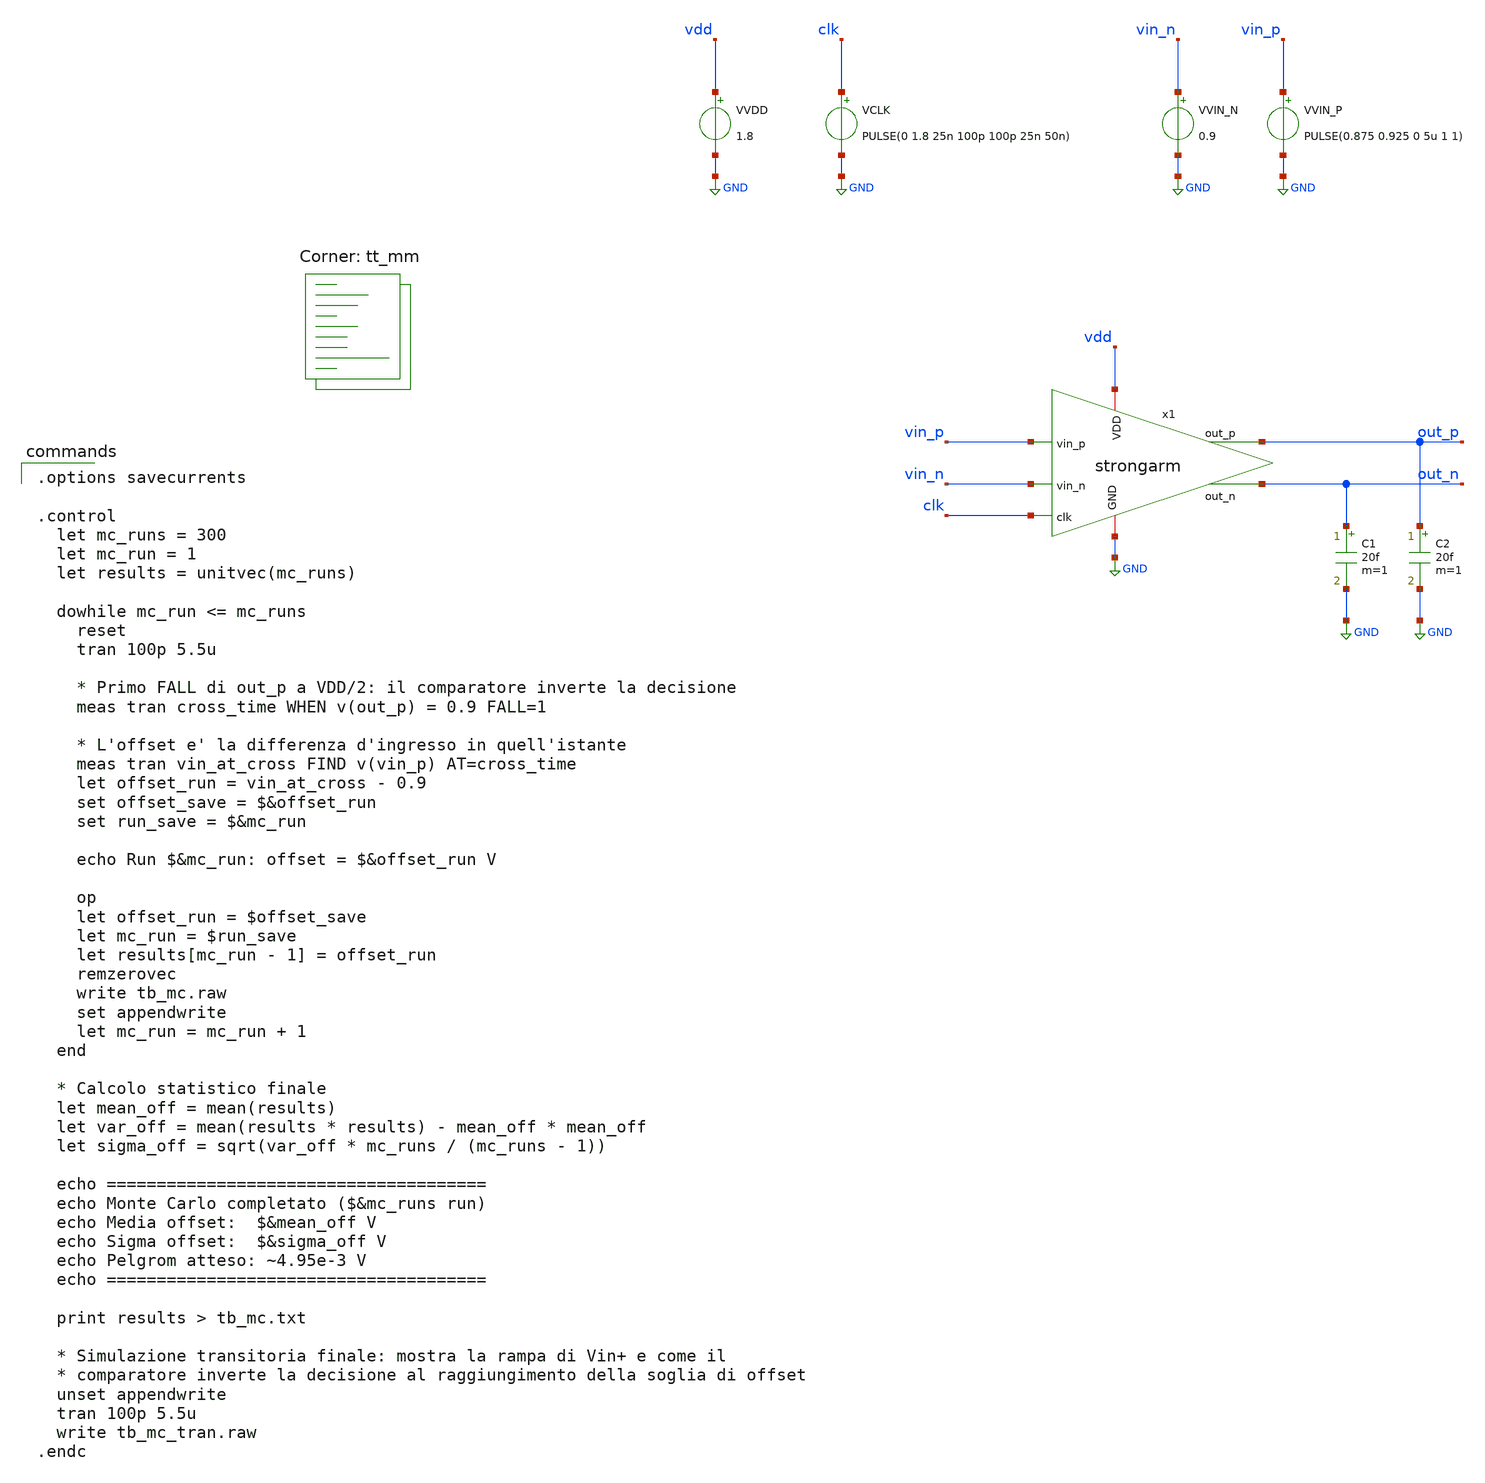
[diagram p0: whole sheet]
** sch_path: 01_xschem_ngspice/soluzioni/lab03/xschem/tb_mc.sch
**.subckt tb_mc
x1 vdd out_p out_n vin_p vin_n clk GND strongarm
VVDD vdd GND 1.8
VCLK clk GND PULSE(0 1.8 25n 100p 100p 25n 50n)
VVIN_P vin_p GND PULSE(0.875 0.925 0 5u 1 1)
VVIN_N vin_n GND 0.9
C1 out_n GND 20f m=1
C2 out_p GND 20f m=1
**** begin user architecture code

.options savecurrents

.control
  let mc_runs = 300
  let mc_run = 1
  let results = unitvec(mc_runs)

  dowhile mc_run <= mc_runs
    reset
    tran 100p 5.5u

    * Primo FALL di out_p a VDD/2: il comparatore inverte la decisione
    meas tran cross_time WHEN v(out_p) = 0.9 FALL=1

    * L'offset e' la differenza d'ingresso in quell'istante
    meas tran vin_at_cross FIND v(vin_p) AT=cross_time
    let offset_run = vin_at_cross - 0.9
    set offset_save = $&offset_run
    set run_save = $&mc_run

    echo Run $&mc_run: offset = $&offset_run V

    op
    let offset_run = $offset_save
    let mc_run = $run_save
    let results[mc_run - 1] = offset_run
    remzerovec
    write tb_mc.raw
    set appendwrite
    let mc_run = mc_run + 1
  end

  * Calcolo statistico finale
  let mean_off = mean(results)
  let var_off = mean(results * results) - mean_off * mean_off
  let sigma_off = sqrt(var_off * mc_runs / (mc_runs - 1))

  echo ======================================
  echo Monte Carlo completato ($&mc_runs run)
  echo Media offset:  $&mean_off V
  echo Sigma offset:  $&sigma_off V
  echo Pelgrom atteso: ~4.95e-3 V
  echo ======================================

  print results > tb_mc.txt

  * Simulazione transitoria finale: mostra la rampa di Vin+ e come il
  * comparatore inverte la decisione al raggiungimento della soglia di offset
  unset appendwrite
  tran 100p 5.5u
  write tb_mc_tran.raw
.endc

.lib $::SKYWATER_MODELS/sky130.lib.spice tt_mm
**** end user architecture code
**.ends
.GLOBAL GND
.end
